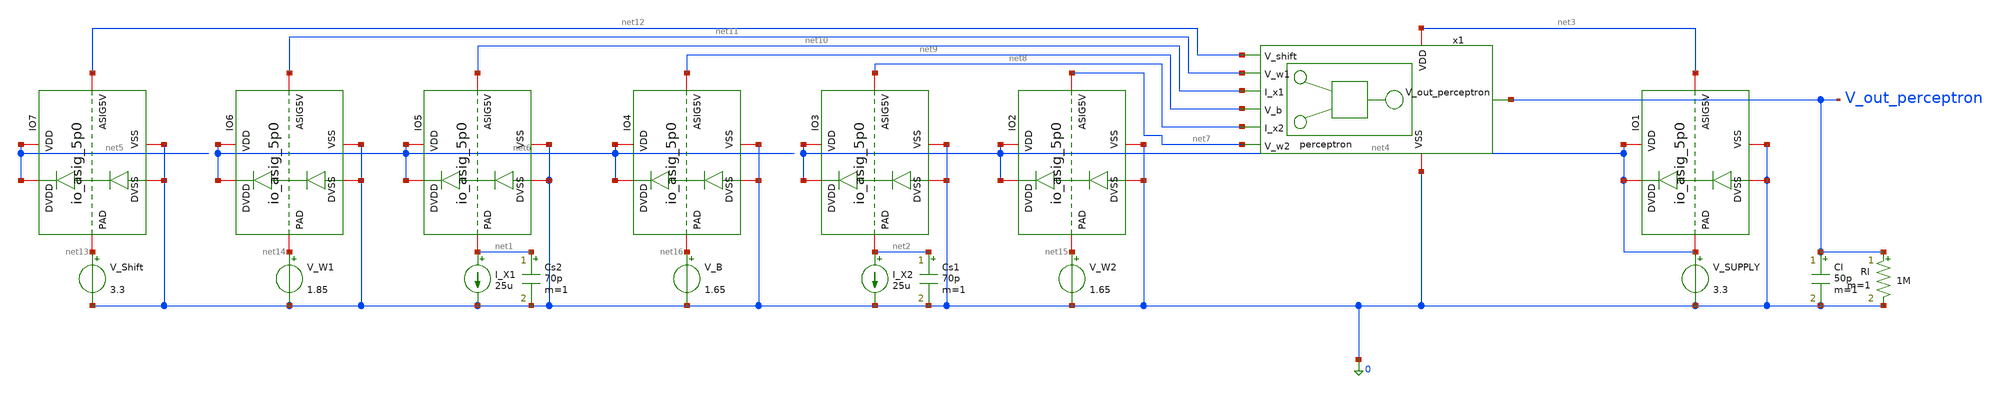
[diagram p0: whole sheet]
** sch_path: lvs/schematics/tb_realistic_perceptron .sch
**.subckt tb_realistic_perceptron
V_SUPPLY net4 0 3.3
V_Shift net13 0 3.3
I_X1 net1 0 25u
I_X2 net2 0 25u
V_W1 net14 0 1.85
V_W2 net15 0 1.65
V_B net16 0 1.65
Cs2 net1 0 70p m=1
Cs1 net2 0 70p m=1
Cl V_out_perceptron 0 50p m=1
Rl V_out_perceptron 0 1M m=1
x1 net3 net12 net11 net10 V_out_perceptron net9 net8 net7 0 perceptron
XIO1 0 net4 0 net4 net4 net3 gf180mcu_fd_io__asig_5p0_extracted
XIO2 0 net4 0 net4 net15 net7 gf180mcu_fd_io__asig_5p0_extracted
XIO3 0 net4 0 net4 net2 net8 gf180mcu_fd_io__asig_5p0_extracted
XIO4 0 net6 0 net6 net16 net9 gf180mcu_fd_io__asig_5p0_extracted
XIO5 0 net6 0 net6 net1 net10 gf180mcu_fd_io__asig_5p0_extracted
XIO6 0 net6 0 net6 net14 net11 gf180mcu_fd_io__asig_5p0_extracted
XIO7 0 net5 0 net5 net13 net12 gf180mcu_fd_io__asig_5p0_extracted
**** begin user architecture code


.control

* --- start from neutral ---
alter V_W1 = 1.65
alter V_W2 = 1.65
alter V_B  = 1.65
alter I_X1 = 0
alter I_X2 = 0
* === Transient Analysis ===
* Applying a 50uA pulse to I_X1 to observe step response and settling
alter @I_X1[pulse] = [ 0 50u 1u 10n 10n 10u 20u ]
alter I_X2 = 0
alter V_W1 = 1.85
alter V_W2 = 1.65
alter V_B  = 1.65
tran 10n 30u
wrdata /foss/designs/analog-perceptron-gf180mcu/plots/real_tran_perceptron.txt v(V_out_perceptron)
destroy all
alter @I_X1[pulse] = [ 0 0 0 0 0 0 0 ] $ Clear pulse after tran
* === AC Analysis (Stability & Bandwidth) ===
* Injecting AC signal into I_X1
alter I_X1 = 25u
alter @I_X1[acmag] = 1
alter V_W1 = 1.85
ac dec 20 1 1G
* wrdata exports real and imaginary parts for AC.
wrdata /foss/designs/analog-perceptron-gf180mcu/plots/real_ac_perceptron.txt v(V_out_perceptron)
destroy all
alter @I_X1[acmag] = 0 $ Clear AC magnitude
alter I_X1 = 0
* === Return to global environment before loops ===
reset
setplot const
* === Graph 1: Weight sweep (inhibitory / neutral / excitatory) ===
alter I_X2 = 0
alter V_W2 = 1.65
alter V_B  = 1.65
let n = 0
dowhile n <= 2
let vw1 = 1.45 + n * 0.2
alter V_W1 = vw1
dc I_X1 0 50u 1u
wrdata /foss/designs/analog-perceptron-gf180mcu/plots/real_perceptron_graph1_weights.txt
+ v(V_out_perceptron)
destroy all
set appendwrite
let n = n + 1
end
unset appendwrite
alter V_W1 = 1.65
* === Graph 2: Sensor 1 sweep, Sensor 2 interference ===
alter V_W1 = 1.85
alter V_W2 = 1.85
alter V_B  = 1.65
let n = 0
dowhile n <= 2
let ix2 = n * 25u
alter I_X2 = ix2
dc I_X1 0 50u 1u
wrdata /foss/designs/analog-perceptron-gf180mcu/plots/real_perceptron_graph2_sensors.txt
+ v(V_out_perceptron)
destroy all
set appendwrite
let n = n + 1
end
unset appendwrite
alter V_W1 = 1.65
alter V_W2 = 1.65
alter I_X2 = 0
* === Graph 3: Bias shifting ===
alter I_X2 = 0
alter V_W1 = 1.85
let n = 0
dowhile n <= 2
let vb = 1.45 + n * 0.2
alter V_B = vb
dc I_X1 0 50u 1u
wrdata /foss/designs/analog-perceptron-gf180mcu/plots/real_perceptron_graph3_bias.txt
+ v(V_out_perceptron)
destroy all
set appendwrite
let n = n + 1
end
unset appendwrite
alter V_W1 = 1.65
alter V_B  = 1.65
* === Graph 4: V_Shift sweep (reference-rail sensitivity / corner check) ===
alter I_X2 = 0
alter V_W1 = 1.85
alter V_B  = 1.65
let n = 0
dowhile n <= 5
let vshift = 3.25 + n * 0.02
alter V_Shift = vshift
dc I_X1 0 50u 1u
wrdata /foss/designs/analog-perceptron-gf180mcu/plots/real_perceptron_graph4_vshift.txt
+ v(V_out_perceptron)
destroy all
set appendwrite
let n = n + 1
end
unset appendwrite
alter V_Shift = 3.3
alter V_W1 = 1.65
* === 3D Dataset A: I_X1 x I_X2 -> V_out ===
alter V_W1 = 1.85
alter V_W2 = 1.85
alter V_B  = 1.65
let n = 0
dowhile n <= 25
let ix2b = n * 2u
alter I_X2 = ix2b
dc I_X1 0 50u 1u
wrdata /foss/designs/analog-perceptron-gf180mcu/plots/real_3d_sensors.txt v(V_out_perceptron)
destroy all
set appendwrite
let n = n + 1
end
unset appendwrite
alter V_W1 = 1.65
alter V_W2 = 1.65
alter I_X2 = 0
* === 3D Dataset B: V_W1 x V_W2 -> V_out ===
alter I_X1 = 50u
alter I_X2 = 50u
alter V_B  = 1.65
let n = 0
dowhile n <= 20
let vw2 = 1.45 + n * 0.02
alter V_W2 = vw2
dc V_W1 1.45 1.85 0.01
wrdata /foss/designs/analog-perceptron-gf180mcu/plots/real_3d_weights.txt v(V_out_perceptron)
destroy all
set appendwrite
let n = n + 1
end
unset appendwrite
alter V_W1 = 1.65
alter V_W2 = 1.65
alter V_B  = 1.65
alter I_X1 = 0
alter I_X2 = 0
* === OP-SWEEP DIAGNOSTIC: all devices ===
alter V_W1 = 1.85
alter V_W2 = 1.65
alter V_B  = 1.65
alter I_X2 = 0
save all @m.x1.x1.x1.xm1.m0[vgs] @m.x1.x1.x1.xm1.m0[vth] @m.x1.x1.x1.xm1.m0[id]
+ @m.x1.x1.x2.xm1.m0[vgs] @m.x1.x1.x2.xm1.m0[vth] @m.x1.x1.x2.xm1.m0[id] @m.x1.x1.x_g1.xm7.m0[vgs] @m.x1.x1.x_g1.xm7.m0[vth]
+ @m.x1.x1.x_g1.xm7.m0[id] @m.x1.x1.x_g2.xm7.m0[vgs] @m.x1.x1.x_g2.xm7.m0[vth] @m.x1.x1.x_g2.xm7.m0[id]
+ @m.x1.x1.x_g3.xm7.m0[vgs] @m.x1.x1.x_g3.xm7.m0[vth] @m.x1.x1.x_g3.xm7.m0[id] @m.x1.x1.x_tanh.xm1.m0[vgs]
+ @m.x1.x1.x_tanh.xm1.m0[vth] @m.x1.x1.x_tanh.xm1.m0[id] @m.x1.x1.x_tanh.xm2.m0[vgs] @m.x1.x1.x_tanh.xm2.m0[vth]
+ @m.x1.x1.x_tanh.xm2.m0[id]
dc I_X1 0 50u 1u
wrdata /foss/designs/analog-perceptron-gf180mcu/plots/real_opsweep_perceptron_chain.txt
+ v(V_out_perceptron) @m.x1.x1.x1.xm1.m0[vgs] @m.x1.x1.x1.xm1.m0[vth] @m.x1.x1.x1.xm1.m0[id] @m.x1.x1.x2.xm1.m0[vgs]
+ @m.x1.x1.x2.xm1.m0[vth] @m.x1.x1.x2.xm1.m0[id] @m.x1.x1.x_g1.xm7.m0[vgs] @m.x1.x1.x_g1.xm7.m0[vth] @m.x1.x1.x_g1.xm7.m0[id]
+ @m.x1.x1.x_g2.xm7.m0[vgs] @m.x1.x1.x_g2.xm7.m0[vth] @m.x1.x1.x_g2.xm7.m0[id] @m.x1.x1.x_g3.xm7.m0[vgs]
+ @m.x1.x1.x_g3.xm7.m0[vth] @m.x1.x1.x_g3.xm7.m0[id] @m.x1.x1.x_tanh.xm1.m0[vgs] @m.x1.x1.x_tanh.xm1.m0[vth]
+ @m.x1.x1.x_tanh.xm1.m0[id] @m.x1.x1.x_tanh.xm2.m0[vgs] @m.x1.x1.x_tanh.xm2.m0[vth] @m.x1.x1.x_tanh.xm2.m0[id]
destroy all
alter V_W1 = 1.65
alter V_W2 = 1.65
alter V_B  = 1.65
alter I_X1 = 0
alter I_X2 = 0
* === OP-SWEEP DIAGNOSTIC #2: all devices, I_X2 swept ===
alter V_W1 = 1.85
alter V_W2 = 1.65
alter V_B  = 1.65
alter I_X1 = 25u
save all @m.x1.x1.x1.xm1.m0[vgs] @m.x1.x1.x1.xm1.m0[vth] @m.x1.x1.x1.xm1.m0[id]
+ @m.x1.x1.x2.xm1.m0[vgs] @m.x1.x1.x2.xm1.m0[vth] @m.x1.x1.x2.xm1.m0[id] @m.x1.x1.x_g1.xm7.m0[vgs] @m.x1.x1.x_g1.xm7.m0[vth]
+ @m.x1.x1.x_g1.xm7.m0[id] @m.x1.x1.x_g2.xm7.m0[vgs] @m.x1.x1.x_g2.xm7.m0[vth] @m.x1.x1.x_g2.xm7.m0[id]
+ @m.x1.x1.x_g3.xm7.m0[vgs] @m.x1.x1.x_g3.xm7.m0[vth] @m.x1.x1.x_g3.xm7.m0[id] @m.x1.x1.x_tanh.xm1.m0[vgs]
+ @m.x1.x1.x_tanh.xm1.m0[vth] @m.x1.x1.x_tanh.xm1.m0[id] @m.x1.x1.x_tanh.xm2.m0[vgs] @m.x1.x1.x_tanh.xm2.m0[vth]
+ @m.x1.x1.x_tanh.xm2.m0[id]
dc I_X2 0 50u 1u
wrdata /foss/designs/analog-perceptron-gf180mcu/plots/real_opsweep_perceptron_chain_ix2.txt
+ v(V_out_perceptron) @m.x1.x1.x1.xm1.m0[vgs] @m.x1.x1.x1.xm1.m0[vth] @m.x1.x1.x1.xm1.m0[id] @m.x1.x1.x2.xm1.m0[vgs]
+ @m.x1.x1.x2.xm1.m0[vth] @m.x1.x1.x2.xm1.m0[id] @m.x1.x1.x_g1.xm7.m0[vgs] @m.x1.x1.x_g1.xm7.m0[vth] @m.x1.x1.x_g1.xm7.m0[id]
+ @m.x1.x1.x_g2.xm7.m0[vgs] @m.x1.x1.x_g2.xm7.m0[vth] @m.x1.x1.x_g2.xm7.m0[id] @m.x1.x1.x_g3.xm7.m0[vgs]
+ @m.x1.x1.x_g3.xm7.m0[vth] @m.x1.x1.x_g3.xm7.m0[id] @m.x1.x1.x_tanh.xm1.m0[vgs] @m.x1.x1.x_tanh.xm1.m0[vth]
+ @m.x1.x1.x_tanh.xm1.m0[id] @m.x1.x1.x_tanh.xm2.m0[vgs] @m.x1.x1.x_tanh.xm2.m0[vth] @m.x1.x1.x_tanh.xm2.m0[id]
destroy all
.endc



.include $::180MCU_MODELS/design.ngspice
.lib $::180MCU_MODELS/sm141064.ngspice typical
.lib $::180MCU_MODELS/sm141064.ngspice res_typical
.lib $::180MCU_MODELS/sm141064.ngspice diode_typical
.lib $::180MCU_MODELS/sm141064.ngspice moscap_typical
* .lib $::180MCU_MODELS/sm141064.ngspice res_statistical
.include /foss/designs/analog-perceptron-gf180mcu/schematics/gf180mcu_fd_io__asig_5p0_extracted.spice

**** end user architecture code
**.ends
.end
